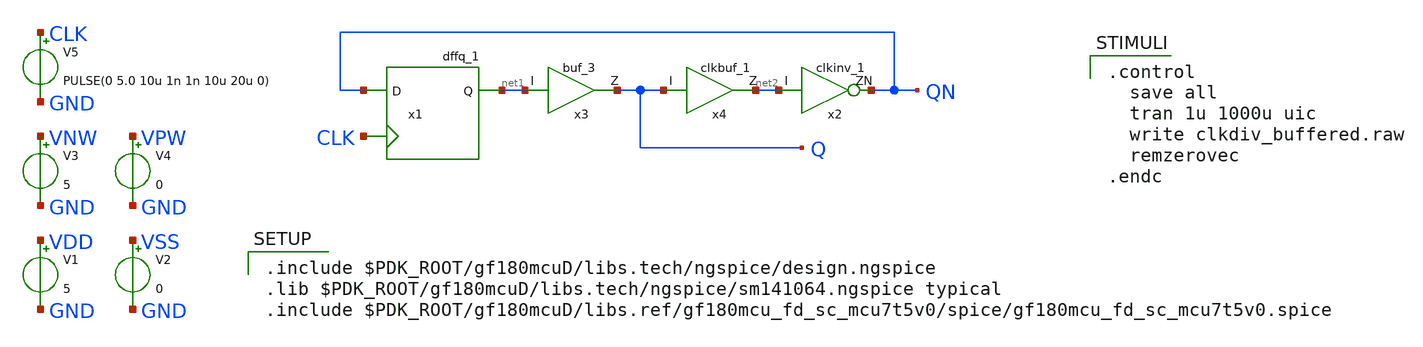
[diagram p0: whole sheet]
** sch_path: clkdiv_buffered.sch
**.subckt clkdiv_buffered
V1 VDD GND 5
V2 VSS GND 0
V3 VNW GND 5
V4 VPW GND 0
V5 CLK GND PULSE(0 5.0 10u 1n 1n 10u 20u 0)
x1 QN CLK net1 VDD VNW VPW VSS gf180mcu_fd_sc_mcu7t5v0__dffq_1
x2 net2 QN VDD VNW VPW VSS gf180mcu_fd_sc_mcu7t5v0__clkinv_1
x3 net1 Q VDD VNW VPW VSS gf180mcu_fd_sc_mcu7t5v0__buf_3
x4 Q net2 VDD VNW VPW VSS gf180mcu_fd_sc_mcu7t5v0__clkbuf_1
**** begin user architecture code

.include $PDK_ROOT/gf180mcuD/libs.tech/ngspice/design.ngspice
.lib $PDK_ROOT/gf180mcuD/libs.tech/ngspice/sm141064.ngspice typical
.include $PDK_ROOT/gf180mcuD/libs.ref/gf180mcu_fd_sc_mcu7t5v0/spice/gf180mcu_fd_sc_mcu7t5v0.spice


.control
  save all
  tran 1u 1000u uic
  write clkdiv_buffered.raw
  remzerovec
.endc

**** end user architecture code
**.ends
.end
